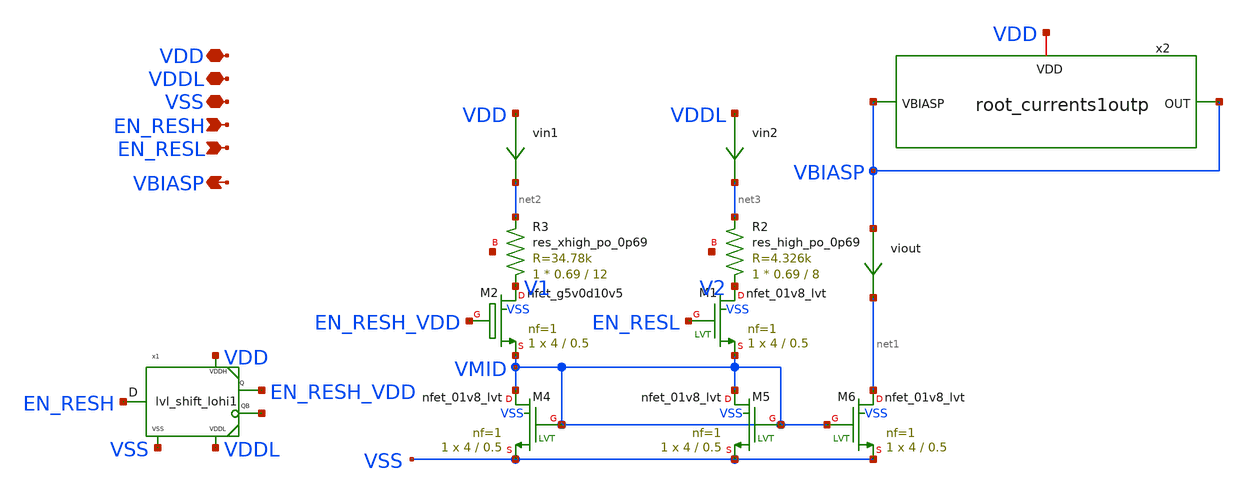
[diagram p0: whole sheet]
** sch_path: xschem/root_currents1.sch
**.subckt root_currents1 VSS EN_RESH VBIASP VDDL VDD EN_RESL
*.iopin VSS
*.ipin EN_RESH
*.opin VBIASP
*.iopin VDDL
*.iopin VDD
*.ipin EN_RESL
XR2 V2 net3 net4 sky130_fd_pr__res_high_po_0p69 L=8 mult=1 m=1
XM4 VMID VMID VSS VSS sky130_fd_pr__nfet_01v8_lvt L=0.5 W=4 nf=1 ad='int((nf+1)/2) * W/nf * 0.29' as='int((nf+2)/2) * W/nf * 0.29'
+ pd='2*int((nf+1)/2) * (W/nf + 0.29)' ps='2*int((nf+2)/2) * (W/nf + 0.29)' nrd='0.29 / W' nrs='0.29 / W'
+ sa=0 sb=0 sd=0 mult=1 m=1
XM5 VMID VMID VSS VSS sky130_fd_pr__nfet_01v8_lvt L=0.5 W=4 nf=1 ad='int((nf+1)/2) * W/nf * 0.29' as='int((nf+2)/2) * W/nf * 0.29'
+ pd='2*int((nf+1)/2) * (W/nf + 0.29)' ps='2*int((nf+2)/2) * (W/nf + 0.29)' nrd='0.29 / W' nrs='0.29 / W'
+ sa=0 sb=0 sd=0 mult=1 m=1
XM6 net1 VMID VSS VSS sky130_fd_pr__nfet_01v8_lvt L=0.5 W=4 nf=1 ad='int((nf+1)/2) * W/nf * 0.29' as='int((nf+2)/2) * W/nf * 0.29'
+ pd='2*int((nf+1)/2) * (W/nf + 0.29)' ps='2*int((nf+2)/2) * (W/nf + 0.29)' nrd='0.29 / W' nrs='0.29 / W'
+ sa=0 sb=0 sd=0 mult=1 m=1
XM2 V1 EN_RESH_VDD VMID VSS sky130_fd_pr__nfet_g5v0d10v5 L=0.5 W=4 nf=1 ad='int((nf+1)/2) * W/nf * 0.29'
+ as='int((nf+2)/2) * W/nf * 0.29' pd='2*int((nf+1)/2) * (W/nf + 0.29)' ps='2*int((nf+2)/2) * (W/nf + 0.29)'
+ nrd='0.29 / W' nrs='0.29 / W' sa=0 sb=0 sd=0 mult=1 m=1
viout VBIASP net1 0
.save i(viout)
x1 EN_RESH EN_RESH_VDD net5 VDD VDDL VSS lvl_shift_lohi1
vin1 VDD net2 0
.save i(vin1)
vin2 VDDL net3 0
.save i(vin2)
XM1 V2 EN_RESL VMID VSS sky130_fd_pr__nfet_01v8_lvt L=0.5 W=4 nf=1 ad='int((nf+1)/2) * W/nf * 0.29' as='int((nf+2)/2) * W/nf * 0.29'
+ pd='2*int((nf+1)/2) * (W/nf + 0.29)' ps='2*int((nf+2)/2) * (W/nf + 0.29)' nrd='0.29 / W' nrs='0.29 / W'
+ sa=0 sb=0 sd=0 mult=1 m=1
x2 VBIASP VBIASP VDD root_currents1outp
XR3 V1 net2 net6 sky130_fd_pr__res_xhigh_po_0p69 L=12 mult=1 m=1
**.ends

* expanding   symbol:  lvl_shift_lohi1.sym # of pins=6
** sym_path: xschem/lvl_shift_lohi1.sym
** sch_path: xschem/lvl_shift_lohi1.sch
.subckt lvl_shift_lohi1 D Q QB VDDH VDDL VSS
*.ipin D
*.opin Q
*.opin QB
*.iopin VDDH
*.iopin VDDL
*.iopin VSS
vpwr VDDL net1 0
.save i(vpwr)
XM1 QB Q VDDH VDDH sky130_fd_pr__pfet_g5v0d10v5 L=0.5 W=2 nf=1 ad='int((nf+1)/2) * W/nf * 0.29' as='int((nf+2)/2) * W/nf * 0.29'
+ pd='2*int((nf+1)/2) * (W/nf + 0.29)' ps='2*int((nf+2)/2) * (W/nf + 0.29)' nrd='0.29 / W' nrs='0.29 / W'
+ sa=0 sb=0 sd=0 mult=1 m=1
XM2 Q QB VDDH VDDH sky130_fd_pr__pfet_g5v0d10v5 L=0.5 W=2 nf=1 ad='int((nf+1)/2) * W/nf * 0.29' as='int((nf+2)/2) * W/nf * 0.29'
+ pd='2*int((nf+1)/2) * (W/nf + 0.29)' ps='2*int((nf+2)/2) * (W/nf + 0.29)' nrd='0.29 / W' nrs='0.29 / W'
+ sa=0 sb=0 sd=0 mult=1 m=1
XM3 QB D VSS VSS sky130_fd_pr__nfet_g5v0d10v5 L=0.5 W=4 nf=1 ad='int((nf+1)/2) * W/nf * 0.29' as='int((nf+2)/2) * W/nf * 0.29'
+ pd='2*int((nf+1)/2) * (W/nf + 0.29)' ps='2*int((nf+2)/2) * (W/nf + 0.29)' nrd='0.29 / W' nrs='0.29 / W'
+ sa=0 sb=0 sd=0 mult=1 m=1
XM4 Q DB VSS VSS sky130_fd_pr__nfet_g5v0d10v5 L=0.5 W=4 nf=1 ad='int((nf+1)/2) * W/nf * 0.29' as='int((nf+2)/2) * W/nf * 0.29'
+ pd='2*int((nf+1)/2) * (W/nf + 0.29)' ps='2*int((nf+2)/2) * (W/nf + 0.29)' nrd='0.29 / W' nrs='0.29 / W'
+ sa=0 sb=0 sd=0 mult=1 m=1
XM5 DB D VSS VSS sky130_fd_pr__nfet_01v8_lvt L=0.5 W=1 nf=1 ad='int((nf+1)/2) * W/nf * 0.29' as='int((nf+2)/2) * W/nf * 0.29'
+ pd='2*int((nf+1)/2) * (W/nf + 0.29)' ps='2*int((nf+2)/2) * (W/nf + 0.29)' nrd='0.29 / W' nrs='0.29 / W'
+ sa=0 sb=0 sd=0 mult=1 m=1
XM6 DB D net1 VDDL sky130_fd_pr__pfet_01v8_lvt L=0.5 W=2 nf=1 ad='int((nf+1)/2) * W/nf * 0.29' as='int((nf+2)/2) * W/nf * 0.29'
+ pd='2*int((nf+1)/2) * (W/nf + 0.29)' ps='2*int((nf+2)/2) * (W/nf + 0.29)' nrd='0.29 / W' nrs='0.29 / W'
+ sa=0 sb=0 sd=0 mult=1 m=1
.ends


* expanding   symbol:  root_currents1outp.sym # of pins=3
** sym_path: xschem/root_currents1outp.sym
** sch_path: xschem/root_currents1outp.sch
.subckt root_currents1outp VBIASP OUT VDD
*.iopin VBIASP
*.iopin OUT
*.iopin VDD
XM7 net1 VBIASP VDD VDD sky130_fd_pr__pfet_g5v0d10v5 L=0.5 W=4 nf=1 ad='int((nf+1)/2) * W/nf * 0.29'
+ as='int((nf+2)/2) * W/nf * 0.29' pd='2*int((nf+1)/2) * (W/nf + 0.29)' ps='2*int((nf+2)/2) * (W/nf + 0.29)'
+ nrd='0.29 / W' nrs='0.29 / W' sa=0 sb=0 sd=0 mult=1 m=1
viout net1 OUT 0
.save i(viout)
.ends

.end
